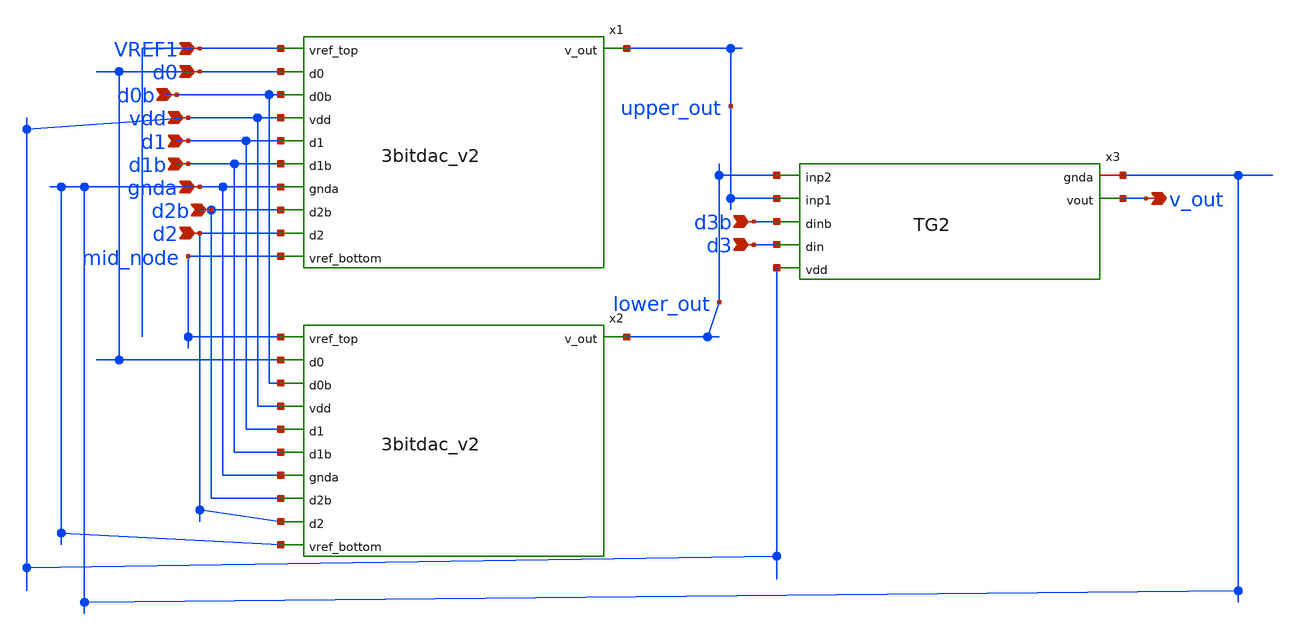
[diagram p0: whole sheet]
** sch_path: prelayout/4bitdac.sch
**.subckt 4bitdac VREF1 gnda vdd d3 d3b d2 d2b d1 d1b d0 d0b v_out
*.ipin VREF1
*.ipin gnda
*.ipin vdd
*.ipin d3
*.ipin d3b
*.ipin d2
*.ipin d2b
*.ipin d1
*.ipin d1b
*.ipin d0
*.ipin d0b
*.opin v_out
Xx3 gnda v_out lower_out upper_out d3b d3 vdd TG2
x1 VREF1 d0 d0b vdd d1 d1b upper_out gnda d2b d2 mid_node 3bitdac_v2
x2 mid_node d0 d0b vdd d1 d1b lower_out gnda d2b d2 gnda 3bitdac_v2
**.ends
.end
